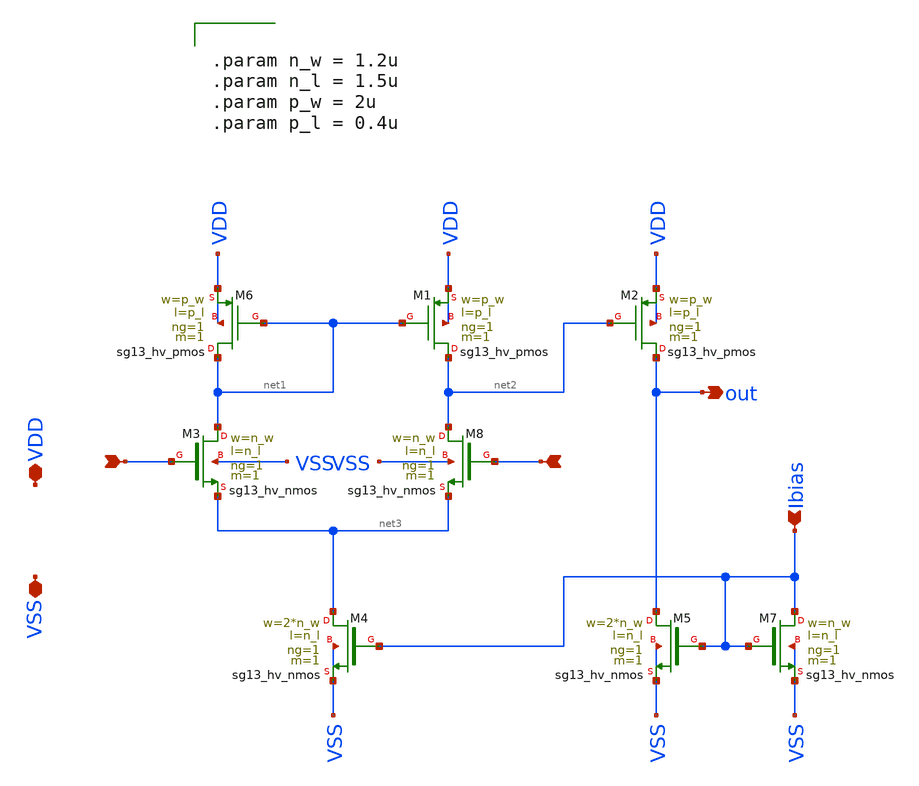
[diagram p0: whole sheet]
** sch_path: macros/heichips26_vcr/macros/switched_capacitor/schematic/xschem/comp_nmos.sch
**.subckt comp_nmos VDD VSS - + Ibias out
*.iopin VDD
*.iopin VSS
*.ipin -
*.ipin +
*.ipin Ibias
*.opin out
XM8 net2 + net3 VSS sg13_hv_nmos w=n_w l=n_l ng=1 m=1 mm_ok=1
XM6 net1 net1 VDD VDD sg13_hv_pmos w=p_w l=p_l ng=1 m=1 mm_ok=1
XM1 net2 net1 VDD VDD sg13_hv_pmos w=p_w l=p_l ng=1 m=1 mm_ok=1
XM3 net1 - net3 VSS sg13_hv_nmos w=n_w l=n_l ng=1 m=1 mm_ok=1
XM2 out net2 VDD VDD sg13_hv_pmos w=p_w l=p_l ng=1 m=1 mm_ok=1
XM4 net3 Ibias VSS VSS sg13_hv_nmos w=2*n_w l=n_l ng=1 m=1 mm_ok=1
XM5 out Ibias VSS VSS sg13_hv_nmos w=2*n_w l=n_l ng=1 m=1 mm_ok=1
XM7 Ibias Ibias VSS VSS sg13_hv_nmos w=n_w l=n_l ng=1 m=1 mm_ok=1
**** begin user architecture code


.param n_w = 1.2u
.param n_l = 1.5u
.param p_w = 2u
.param p_l = 0.4u


**** end user architecture code
**.ends
.end
